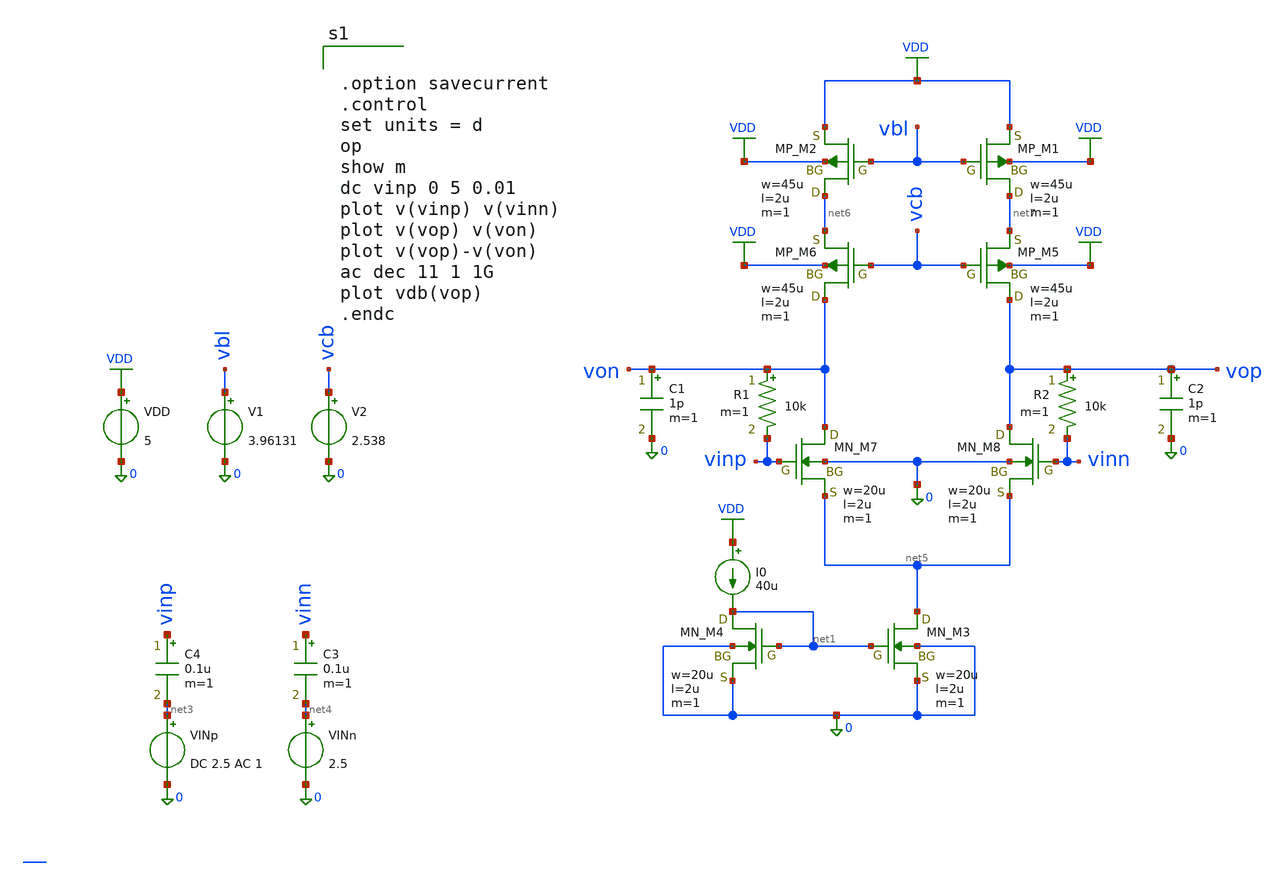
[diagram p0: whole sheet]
** sch_path: member_project/JJY_Receiver/Masahiro/jjy_recv/diff_amp/diff_cascode_nin.sch
**.subckt diff_cascode_nin
VDD VDD 0 5
VINp net3 0 DC 2.5 AC 1
I0 VDD net1 40u
C1 von 0 1p m=1
V1 vbl 0 3.96131
XM1 net7 vbl VDD VDD PMOS w=45u l=2u as=0 ad=0 ps=0 pd=0 nrd=0 nrs=0 m=1
XM2 net6 vbl VDD VDD PMOS w=45u l=2u as=0 ad=0 ps=0 pd=0 nrd=0 nrs=0 m=1
XM3 net5 net1 0 0 NMOS w=20u l=2u as=0 ad=0 ps=0 pd=0 nrd=0 nrs=0 m=1
XM4 net1 net1 0 0 NMOS w=20u l=2u as=0 ad=0 ps=0 pd=0 nrd=0 nrs=0 m=1
C2 vop 0 1p m=1
VINn net4 0 2.5
XM7 von vinp net5 0 NMOS w=20u l=2u as=0 ad=0 ps=0 pd=0 nrd=0 nrs=0 m=1
XM8 vop vinn net5 0 NMOS w=20u l=2u as=0 ad=0 ps=0 pd=0 nrd=0 nrs=0 m=1
XM5 vop vcb net7 VDD PMOS w=45u l=2u as=0 ad=0 ps=0 pd=0 nrd=0 nrs=0 m=1
XM6 von vcb net6 VDD PMOS w=45u l=2u as=0 ad=0 ps=0 pd=0 nrd=0 nrs=0 m=1
V2 vcb 0 2.538
R1 von vinp 10k m=1
R2 vop vinn 10k m=1
C3 vinn net4 0.1u m=1
C4 vinp net3 0.1u m=1
**** begin user architecture code
 .include $::LIB/ip62_models


.option savecurrent
.control
set units = d
op
show m
dc vinp 0 5 0.01
plot v(vinp) v(vinn)
plot v(vop) v(von)
plot v(vop)-v(von)
ac dec 11 1 1G
plot vdb(vop)
.endc


**** end user architecture code
**.ends
.GLOBAL VDD
.end
